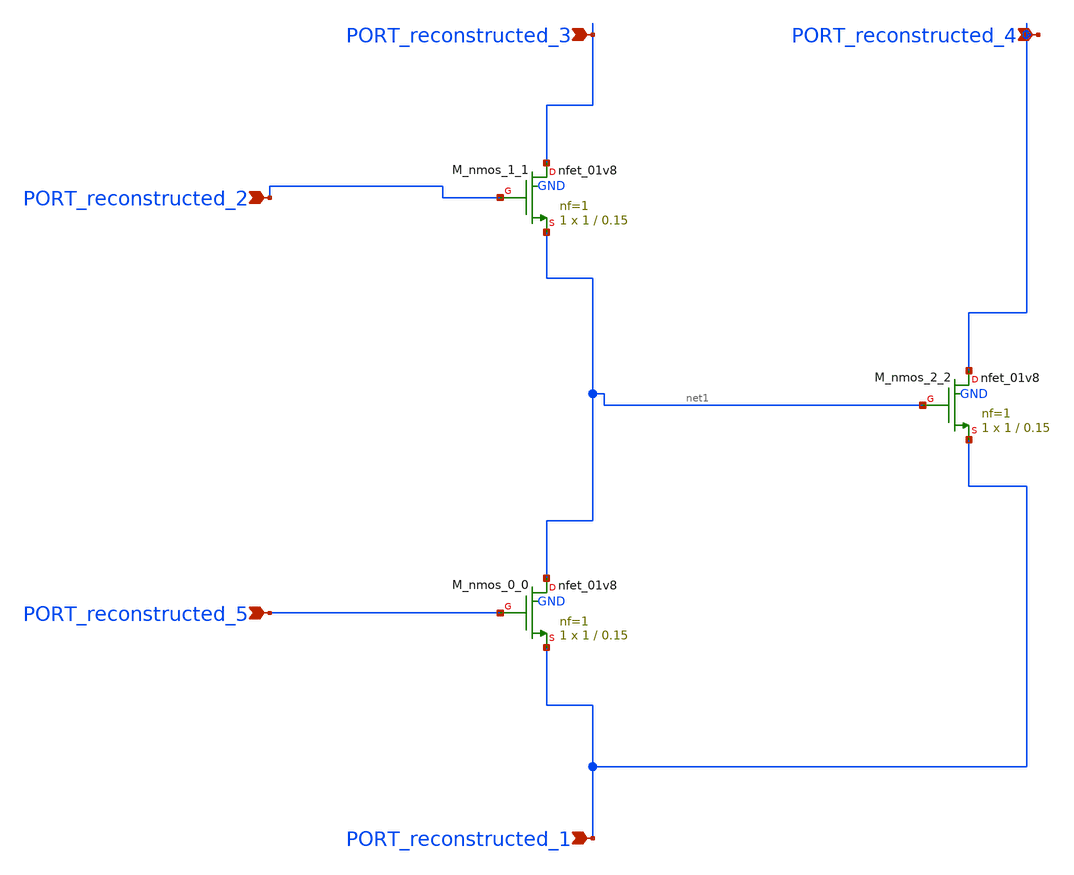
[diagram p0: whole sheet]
** sch_path: schematics/AMSNet/13.sch
**.subckt 13 PORT_reconstructed_5 PORT_reconstructed_1 PORT_reconstructed_2 PORT_reconstructed_3
*+ PORT_reconstructed_4
*.ipin PORT_reconstructed_5
*.ipin PORT_reconstructed_1
*.ipin PORT_reconstructed_2
*.ipin PORT_reconstructed_3
*.ipin PORT_reconstructed_4
XM_nmos_0_0 net1 PORT_reconstructed_5 PORT_reconstructed_1 GND sky130_fd_pr__nfet_01v8 L=0.15 W=1 nf=1
+ ad='int((1 + 1)/2) * 1 / 1 * 0.29' as='int((1 + 2)/2) * 1 / 1 * 0.29' pd='2*int((1 + 1)/2) * (1 / 1 + 0.29)'
+ ps='2*int((1 + 2)/2) * (1 / 1 + 0.29)' nrd='0.29 / 1 ' nrs='0.29 / 1 ' sa=0 sb=0 sd=0 mult=1 m=1
XM_nmos_1_1 PORT_reconstructed_3 PORT_reconstructed_2 net1 GND sky130_fd_pr__nfet_01v8 L=0.15 W=1 nf=1
+ ad='int((1 + 1)/2) * 1 / 1 * 0.29' as='int((1 + 2)/2) * 1 / 1 * 0.29' pd='2*int((1 + 1)/2) * (1 / 1 + 0.29)'
+ ps='2*int((1 + 2)/2) * (1 / 1 + 0.29)' nrd='0.29 / 1 ' nrs='0.29 / 1 ' sa=0 sb=0 sd=0 mult=1 m=1
XM_nmos_2_2 PORT_reconstructed_4 net1 PORT_reconstructed_1 GND sky130_fd_pr__nfet_01v8 L=0.15 W=1 nf=1
+ ad='int((1 + 1)/2) * 1 / 1 * 0.29' as='int((1 + 2)/2) * 1 / 1 * 0.29' pd='2*int((1 + 1)/2) * (1 / 1 + 0.29)'
+ ps='2*int((1 + 2)/2) * (1 / 1 + 0.29)' nrd='0.29 / 1 ' nrs='0.29 / 1 ' sa=0 sb=0 sd=0 mult=1 m=1
**.ends
.end
